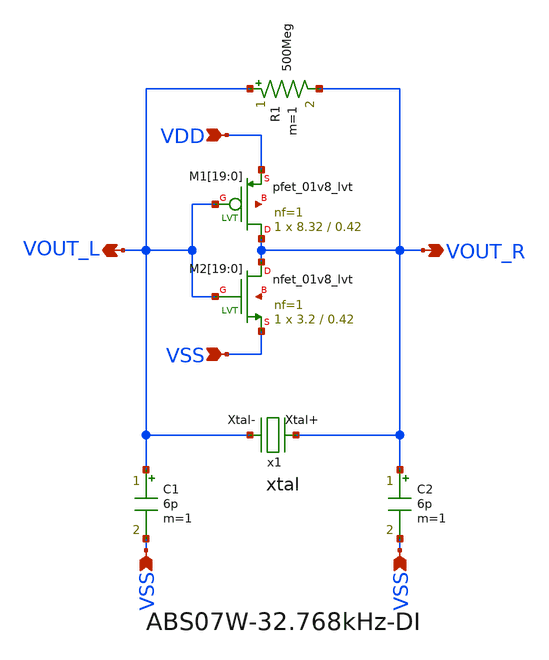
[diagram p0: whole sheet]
** sch_path: design/THESIS_EXP_RO_INVERTER_SKY130A/xtal_osc.sch
**.subckt xtal_osc VDD VSS VSS VSS VOUT_R VOUT_L
*.ipin VDD
*.ipin VSS
*.ipin VSS
*.ipin VSS
*.opin VOUT_R
*.opin VOUT_L
x1 VOUT_R VOUT_L xtal
C1 VOUT_L VSS 6p m=1
C2 VOUT_R VSS 6p m=1
R1 VOUT_L VOUT_R 500Meg m=1
XM1[19] VOUT_R VOUT_L VDD net1[19] sky130_fd_pr__pfet_01v8_lvt L=0.42 W=8.32 nf=1 ad='int((nf+1)/2) * W/nf * 0.29'
+ as='int((nf+2)/2) * W/nf * 0.29' pd='2*int((nf+1)/2) * (W/nf + 0.29)' ps='2*int((nf+2)/2) * (W/nf + 0.29)'
+ nrd='0.29 / W' nrs='0.29 / W' sa=0 sb=0 sd=0 mult=1 m=1
XM1[18] VOUT_R VOUT_L VDD net1[18] sky130_fd_pr__pfet_01v8_lvt L=0.42 W=8.32 nf=1 ad='int((nf+1)/2) * W/nf * 0.29'
+ as='int((nf+2)/2) * W/nf * 0.29' pd='2*int((nf+1)/2) * (W/nf + 0.29)' ps='2*int((nf+2)/2) * (W/nf + 0.29)'
+ nrd='0.29 / W' nrs='0.29 / W' sa=0 sb=0 sd=0 mult=1 m=1
XM1[17] VOUT_R VOUT_L VDD net1[17] sky130_fd_pr__pfet_01v8_lvt L=0.42 W=8.32 nf=1 ad='int((nf+1)/2) * W/nf * 0.29'
+ as='int((nf+2)/2) * W/nf * 0.29' pd='2*int((nf+1)/2) * (W/nf + 0.29)' ps='2*int((nf+2)/2) * (W/nf + 0.29)'
+ nrd='0.29 / W' nrs='0.29 / W' sa=0 sb=0 sd=0 mult=1 m=1
XM1[16] VOUT_R VOUT_L VDD net1[16] sky130_fd_pr__pfet_01v8_lvt L=0.42 W=8.32 nf=1 ad='int((nf+1)/2) * W/nf * 0.29'
+ as='int((nf+2)/2) * W/nf * 0.29' pd='2*int((nf+1)/2) * (W/nf + 0.29)' ps='2*int((nf+2)/2) * (W/nf + 0.29)'
+ nrd='0.29 / W' nrs='0.29 / W' sa=0 sb=0 sd=0 mult=1 m=1
XM1[15] VOUT_R VOUT_L VDD net1[15] sky130_fd_pr__pfet_01v8_lvt L=0.42 W=8.32 nf=1 ad='int((nf+1)/2) * W/nf * 0.29'
+ as='int((nf+2)/2) * W/nf * 0.29' pd='2*int((nf+1)/2) * (W/nf + 0.29)' ps='2*int((nf+2)/2) * (W/nf + 0.29)'
+ nrd='0.29 / W' nrs='0.29 / W' sa=0 sb=0 sd=0 mult=1 m=1
XM1[14] VOUT_R VOUT_L VDD net1[14] sky130_fd_pr__pfet_01v8_lvt L=0.42 W=8.32 nf=1 ad='int((nf+1)/2) * W/nf * 0.29'
+ as='int((nf+2)/2) * W/nf * 0.29' pd='2*int((nf+1)/2) * (W/nf + 0.29)' ps='2*int((nf+2)/2) * (W/nf + 0.29)'
+ nrd='0.29 / W' nrs='0.29 / W' sa=0 sb=0 sd=0 mult=1 m=1
XM1[13] VOUT_R VOUT_L VDD net1[13] sky130_fd_pr__pfet_01v8_lvt L=0.42 W=8.32 nf=1 ad='int((nf+1)/2) * W/nf * 0.29'
+ as='int((nf+2)/2) * W/nf * 0.29' pd='2*int((nf+1)/2) * (W/nf + 0.29)' ps='2*int((nf+2)/2) * (W/nf + 0.29)'
+ nrd='0.29 / W' nrs='0.29 / W' sa=0 sb=0 sd=0 mult=1 m=1
XM1[12] VOUT_R VOUT_L VDD net1[12] sky130_fd_pr__pfet_01v8_lvt L=0.42 W=8.32 nf=1 ad='int((nf+1)/2) * W/nf * 0.29'
+ as='int((nf+2)/2) * W/nf * 0.29' pd='2*int((nf+1)/2) * (W/nf + 0.29)' ps='2*int((nf+2)/2) * (W/nf + 0.29)'
+ nrd='0.29 / W' nrs='0.29 / W' sa=0 sb=0 sd=0 mult=1 m=1
XM1[11] VOUT_R VOUT_L VDD net1[11] sky130_fd_pr__pfet_01v8_lvt L=0.42 W=8.32 nf=1 ad='int((nf+1)/2) * W/nf * 0.29'
+ as='int((nf+2)/2) * W/nf * 0.29' pd='2*int((nf+1)/2) * (W/nf + 0.29)' ps='2*int((nf+2)/2) * (W/nf + 0.29)'
+ nrd='0.29 / W' nrs='0.29 / W' sa=0 sb=0 sd=0 mult=1 m=1
XM1[10] VOUT_R VOUT_L VDD net1[10] sky130_fd_pr__pfet_01v8_lvt L=0.42 W=8.32 nf=1 ad='int((nf+1)/2) * W/nf * 0.29'
+ as='int((nf+2)/2) * W/nf * 0.29' pd='2*int((nf+1)/2) * (W/nf + 0.29)' ps='2*int((nf+2)/2) * (W/nf + 0.29)'
+ nrd='0.29 / W' nrs='0.29 / W' sa=0 sb=0 sd=0 mult=1 m=1
XM1[9] VOUT_R VOUT_L VDD net1[9] sky130_fd_pr__pfet_01v8_lvt L=0.42 W=8.32 nf=1 ad='int((nf+1)/2) * W/nf * 0.29'
+ as='int((nf+2)/2) * W/nf * 0.29' pd='2*int((nf+1)/2) * (W/nf + 0.29)' ps='2*int((nf+2)/2) * (W/nf + 0.29)'
+ nrd='0.29 / W' nrs='0.29 / W' sa=0 sb=0 sd=0 mult=1 m=1
XM1[8] VOUT_R VOUT_L VDD net1[8] sky130_fd_pr__pfet_01v8_lvt L=0.42 W=8.32 nf=1 ad='int((nf+1)/2) * W/nf * 0.29'
+ as='int((nf+2)/2) * W/nf * 0.29' pd='2*int((nf+1)/2) * (W/nf + 0.29)' ps='2*int((nf+2)/2) * (W/nf + 0.29)'
+ nrd='0.29 / W' nrs='0.29 / W' sa=0 sb=0 sd=0 mult=1 m=1
XM1[7] VOUT_R VOUT_L VDD net1[7] sky130_fd_pr__pfet_01v8_lvt L=0.42 W=8.32 nf=1 ad='int((nf+1)/2) * W/nf * 0.29'
+ as='int((nf+2)/2) * W/nf * 0.29' pd='2*int((nf+1)/2) * (W/nf + 0.29)' ps='2*int((nf+2)/2) * (W/nf + 0.29)'
+ nrd='0.29 / W' nrs='0.29 / W' sa=0 sb=0 sd=0 mult=1 m=1
XM1[6] VOUT_R VOUT_L VDD net1[6] sky130_fd_pr__pfet_01v8_lvt L=0.42 W=8.32 nf=1 ad='int((nf+1)/2) * W/nf * 0.29'
+ as='int((nf+2)/2) * W/nf * 0.29' pd='2*int((nf+1)/2) * (W/nf + 0.29)' ps='2*int((nf+2)/2) * (W/nf + 0.29)'
+ nrd='0.29 / W' nrs='0.29 / W' sa=0 sb=0 sd=0 mult=1 m=1
XM1[5] VOUT_R VOUT_L VDD net1[5] sky130_fd_pr__pfet_01v8_lvt L=0.42 W=8.32 nf=1 ad='int((nf+1)/2) * W/nf * 0.29'
+ as='int((nf+2)/2) * W/nf * 0.29' pd='2*int((nf+1)/2) * (W/nf + 0.29)' ps='2*int((nf+2)/2) * (W/nf + 0.29)'
+ nrd='0.29 / W' nrs='0.29 / W' sa=0 sb=0 sd=0 mult=1 m=1
XM1[4] VOUT_R VOUT_L VDD net1[4] sky130_fd_pr__pfet_01v8_lvt L=0.42 W=8.32 nf=1 ad='int((nf+1)/2) * W/nf * 0.29'
+ as='int((nf+2)/2) * W/nf * 0.29' pd='2*int((nf+1)/2) * (W/nf + 0.29)' ps='2*int((nf+2)/2) * (W/nf + 0.29)'
+ nrd='0.29 / W' nrs='0.29 / W' sa=0 sb=0 sd=0 mult=1 m=1
XM1[3] VOUT_R VOUT_L VDD net1[3] sky130_fd_pr__pfet_01v8_lvt L=0.42 W=8.32 nf=1 ad='int((nf+1)/2) * W/nf * 0.29'
+ as='int((nf+2)/2) * W/nf * 0.29' pd='2*int((nf+1)/2) * (W/nf + 0.29)' ps='2*int((nf+2)/2) * (W/nf + 0.29)'
+ nrd='0.29 / W' nrs='0.29 / W' sa=0 sb=0 sd=0 mult=1 m=1
XM1[2] VOUT_R VOUT_L VDD net1[2] sky130_fd_pr__pfet_01v8_lvt L=0.42 W=8.32 nf=1 ad='int((nf+1)/2) * W/nf * 0.29'
+ as='int((nf+2)/2) * W/nf * 0.29' pd='2*int((nf+1)/2) * (W/nf + 0.29)' ps='2*int((nf+2)/2) * (W/nf + 0.29)'
+ nrd='0.29 / W' nrs='0.29 / W' sa=0 sb=0 sd=0 mult=1 m=1
XM1[1] VOUT_R VOUT_L VDD net1[1] sky130_fd_pr__pfet_01v8_lvt L=0.42 W=8.32 nf=1 ad='int((nf+1)/2) * W/nf * 0.29'
+ as='int((nf+2)/2) * W/nf * 0.29' pd='2*int((nf+1)/2) * (W/nf + 0.29)' ps='2*int((nf+2)/2) * (W/nf + 0.29)'
+ nrd='0.29 / W' nrs='0.29 / W' sa=0 sb=0 sd=0 mult=1 m=1
XM1[0] VOUT_R VOUT_L VDD net1[0] sky130_fd_pr__pfet_01v8_lvt L=0.42 W=8.32 nf=1 ad='int((nf+1)/2) * W/nf * 0.29'
+ as='int((nf+2)/2) * W/nf * 0.29' pd='2*int((nf+1)/2) * (W/nf + 0.29)' ps='2*int((nf+2)/2) * (W/nf + 0.29)'
+ nrd='0.29 / W' nrs='0.29 / W' sa=0 sb=0 sd=0 mult=1 m=1
XM2[19] VOUT_R VOUT_L VSS net2[19] sky130_fd_pr__nfet_01v8_lvt L=0.42 W=3.2 nf=1 ad='int((nf+1)/2) * W/nf * 0.29'
+ as='int((nf+2)/2) * W/nf * 0.29' pd='2*int((nf+1)/2) * (W/nf + 0.29)' ps='2*int((nf+2)/2) * (W/nf + 0.29)'
+ nrd='0.29 / W' nrs='0.29 / W' sa=0 sb=0 sd=0 mult=1 m=1
XM2[18] VOUT_R VOUT_L VSS net2[18] sky130_fd_pr__nfet_01v8_lvt L=0.42 W=3.2 nf=1 ad='int((nf+1)/2) * W/nf * 0.29'
+ as='int((nf+2)/2) * W/nf * 0.29' pd='2*int((nf+1)/2) * (W/nf + 0.29)' ps='2*int((nf+2)/2) * (W/nf + 0.29)'
+ nrd='0.29 / W' nrs='0.29 / W' sa=0 sb=0 sd=0 mult=1 m=1
XM2[17] VOUT_R VOUT_L VSS net2[17] sky130_fd_pr__nfet_01v8_lvt L=0.42 W=3.2 nf=1 ad='int((nf+1)/2) * W/nf * 0.29'
+ as='int((nf+2)/2) * W/nf * 0.29' pd='2*int((nf+1)/2) * (W/nf + 0.29)' ps='2*int((nf+2)/2) * (W/nf + 0.29)'
+ nrd='0.29 / W' nrs='0.29 / W' sa=0 sb=0 sd=0 mult=1 m=1
XM2[16] VOUT_R VOUT_L VSS net2[16] sky130_fd_pr__nfet_01v8_lvt L=0.42 W=3.2 nf=1 ad='int((nf+1)/2) * W/nf * 0.29'
+ as='int((nf+2)/2) * W/nf * 0.29' pd='2*int((nf+1)/2) * (W/nf + 0.29)' ps='2*int((nf+2)/2) * (W/nf + 0.29)'
+ nrd='0.29 / W' nrs='0.29 / W' sa=0 sb=0 sd=0 mult=1 m=1
XM2[15] VOUT_R VOUT_L VSS net2[15] sky130_fd_pr__nfet_01v8_lvt L=0.42 W=3.2 nf=1 ad='int((nf+1)/2) * W/nf * 0.29'
+ as='int((nf+2)/2) * W/nf * 0.29' pd='2*int((nf+1)/2) * (W/nf + 0.29)' ps='2*int((nf+2)/2) * (W/nf + 0.29)'
+ nrd='0.29 / W' nrs='0.29 / W' sa=0 sb=0 sd=0 mult=1 m=1
XM2[14] VOUT_R VOUT_L VSS net2[14] sky130_fd_pr__nfet_01v8_lvt L=0.42 W=3.2 nf=1 ad='int((nf+1)/2) * W/nf * 0.29'
+ as='int((nf+2)/2) * W/nf * 0.29' pd='2*int((nf+1)/2) * (W/nf + 0.29)' ps='2*int((nf+2)/2) * (W/nf + 0.29)'
+ nrd='0.29 / W' nrs='0.29 / W' sa=0 sb=0 sd=0 mult=1 m=1
XM2[13] VOUT_R VOUT_L VSS net2[13] sky130_fd_pr__nfet_01v8_lvt L=0.42 W=3.2 nf=1 ad='int((nf+1)/2) * W/nf * 0.29'
+ as='int((nf+2)/2) * W/nf * 0.29' pd='2*int((nf+1)/2) * (W/nf + 0.29)' ps='2*int((nf+2)/2) * (W/nf + 0.29)'
+ nrd='0.29 / W' nrs='0.29 / W' sa=0 sb=0 sd=0 mult=1 m=1
XM2[12] VOUT_R VOUT_L VSS net2[12] sky130_fd_pr__nfet_01v8_lvt L=0.42 W=3.2 nf=1 ad='int((nf+1)/2) * W/nf * 0.29'
+ as='int((nf+2)/2) * W/nf * 0.29' pd='2*int((nf+1)/2) * (W/nf + 0.29)' ps='2*int((nf+2)/2) * (W/nf + 0.29)'
+ nrd='0.29 / W' nrs='0.29 / W' sa=0 sb=0 sd=0 mult=1 m=1
XM2[11] VOUT_R VOUT_L VSS net2[11] sky130_fd_pr__nfet_01v8_lvt L=0.42 W=3.2 nf=1 ad='int((nf+1)/2) * W/nf * 0.29'
+ as='int((nf+2)/2) * W/nf * 0.29' pd='2*int((nf+1)/2) * (W/nf + 0.29)' ps='2*int((nf+2)/2) * (W/nf + 0.29)'
+ nrd='0.29 / W' nrs='0.29 / W' sa=0 sb=0 sd=0 mult=1 m=1
XM2[10] VOUT_R VOUT_L VSS net2[10] sky130_fd_pr__nfet_01v8_lvt L=0.42 W=3.2 nf=1 ad='int((nf+1)/2) * W/nf * 0.29'
+ as='int((nf+2)/2) * W/nf * 0.29' pd='2*int((nf+1)/2) * (W/nf + 0.29)' ps='2*int((nf+2)/2) * (W/nf + 0.29)'
+ nrd='0.29 / W' nrs='0.29 / W' sa=0 sb=0 sd=0 mult=1 m=1
XM2[9] VOUT_R VOUT_L VSS net2[9] sky130_fd_pr__nfet_01v8_lvt L=0.42 W=3.2 nf=1 ad='int((nf+1)/2) * W/nf * 0.29'
+ as='int((nf+2)/2) * W/nf * 0.29' pd='2*int((nf+1)/2) * (W/nf + 0.29)' ps='2*int((nf+2)/2) * (W/nf + 0.29)'
+ nrd='0.29 / W' nrs='0.29 / W' sa=0 sb=0 sd=0 mult=1 m=1
XM2[8] VOUT_R VOUT_L VSS net2[8] sky130_fd_pr__nfet_01v8_lvt L=0.42 W=3.2 nf=1 ad='int((nf+1)/2) * W/nf * 0.29'
+ as='int((nf+2)/2) * W/nf * 0.29' pd='2*int((nf+1)/2) * (W/nf + 0.29)' ps='2*int((nf+2)/2) * (W/nf + 0.29)'
+ nrd='0.29 / W' nrs='0.29 / W' sa=0 sb=0 sd=0 mult=1 m=1
XM2[7] VOUT_R VOUT_L VSS net2[7] sky130_fd_pr__nfet_01v8_lvt L=0.42 W=3.2 nf=1 ad='int((nf+1)/2) * W/nf * 0.29'
+ as='int((nf+2)/2) * W/nf * 0.29' pd='2*int((nf+1)/2) * (W/nf + 0.29)' ps='2*int((nf+2)/2) * (W/nf + 0.29)'
+ nrd='0.29 / W' nrs='0.29 / W' sa=0 sb=0 sd=0 mult=1 m=1
XM2[6] VOUT_R VOUT_L VSS net2[6] sky130_fd_pr__nfet_01v8_lvt L=0.42 W=3.2 nf=1 ad='int((nf+1)/2) * W/nf * 0.29'
+ as='int((nf+2)/2) * W/nf * 0.29' pd='2*int((nf+1)/2) * (W/nf + 0.29)' ps='2*int((nf+2)/2) * (W/nf + 0.29)'
+ nrd='0.29 / W' nrs='0.29 / W' sa=0 sb=0 sd=0 mult=1 m=1
XM2[5] VOUT_R VOUT_L VSS net2[5] sky130_fd_pr__nfet_01v8_lvt L=0.42 W=3.2 nf=1 ad='int((nf+1)/2) * W/nf * 0.29'
+ as='int((nf+2)/2) * W/nf * 0.29' pd='2*int((nf+1)/2) * (W/nf + 0.29)' ps='2*int((nf+2)/2) * (W/nf + 0.29)'
+ nrd='0.29 / W' nrs='0.29 / W' sa=0 sb=0 sd=0 mult=1 m=1
XM2[4] VOUT_R VOUT_L VSS net2[4] sky130_fd_pr__nfet_01v8_lvt L=0.42 W=3.2 nf=1 ad='int((nf+1)/2) * W/nf * 0.29'
+ as='int((nf+2)/2) * W/nf * 0.29' pd='2*int((nf+1)/2) * (W/nf + 0.29)' ps='2*int((nf+2)/2) * (W/nf + 0.29)'
+ nrd='0.29 / W' nrs='0.29 / W' sa=0 sb=0 sd=0 mult=1 m=1
XM2[3] VOUT_R VOUT_L VSS net2[3] sky130_fd_pr__nfet_01v8_lvt L=0.42 W=3.2 nf=1 ad='int((nf+1)/2) * W/nf * 0.29'
+ as='int((nf+2)/2) * W/nf * 0.29' pd='2*int((nf+1)/2) * (W/nf + 0.29)' ps='2*int((nf+2)/2) * (W/nf + 0.29)'
+ nrd='0.29 / W' nrs='0.29 / W' sa=0 sb=0 sd=0 mult=1 m=1
XM2[2] VOUT_R VOUT_L VSS net2[2] sky130_fd_pr__nfet_01v8_lvt L=0.42 W=3.2 nf=1 ad='int((nf+1)/2) * W/nf * 0.29'
+ as='int((nf+2)/2) * W/nf * 0.29' pd='2*int((nf+1)/2) * (W/nf + 0.29)' ps='2*int((nf+2)/2) * (W/nf + 0.29)'
+ nrd='0.29 / W' nrs='0.29 / W' sa=0 sb=0 sd=0 mult=1 m=1
XM2[1] VOUT_R VOUT_L VSS net2[1] sky130_fd_pr__nfet_01v8_lvt L=0.42 W=3.2 nf=1 ad='int((nf+1)/2) * W/nf * 0.29'
+ as='int((nf+2)/2) * W/nf * 0.29' pd='2*int((nf+1)/2) * (W/nf + 0.29)' ps='2*int((nf+2)/2) * (W/nf + 0.29)'
+ nrd='0.29 / W' nrs='0.29 / W' sa=0 sb=0 sd=0 mult=1 m=1
XM2[0] VOUT_R VOUT_L VSS net2[0] sky130_fd_pr__nfet_01v8_lvt L=0.42 W=3.2 nf=1 ad='int((nf+1)/2) * W/nf * 0.29'
+ as='int((nf+2)/2) * W/nf * 0.29' pd='2*int((nf+1)/2) * (W/nf + 0.29)' ps='2*int((nf+2)/2) * (W/nf + 0.29)'
+ nrd='0.29 / W' nrs='0.29 / W' sa=0 sb=0 sd=0 mult=1 m=1
**.ends

* expanding   symbol:  THESIS_EXP_RO_INVERTER_SKY130A/xtal.sym # of pins=2
** sym_path: design/THESIS_EXP_RO_INVERTER_SKY130A/xtal.sym
** sch_path: design/THESIS_EXP_RO_INVERTER_SKY130A/xtal.sch
.subckt xtal Xtal+ Xtal-
*.iopin Xtal+
*.iopin Xtal-
R1 Xtal+ net1 38.194k m=1
C1 net1 net2 4.68f m=1
L1 net2 Xtal- 5048.571 m=1
C2 Xtal+ Xtal- 1.15p m=1
.ends

.end
